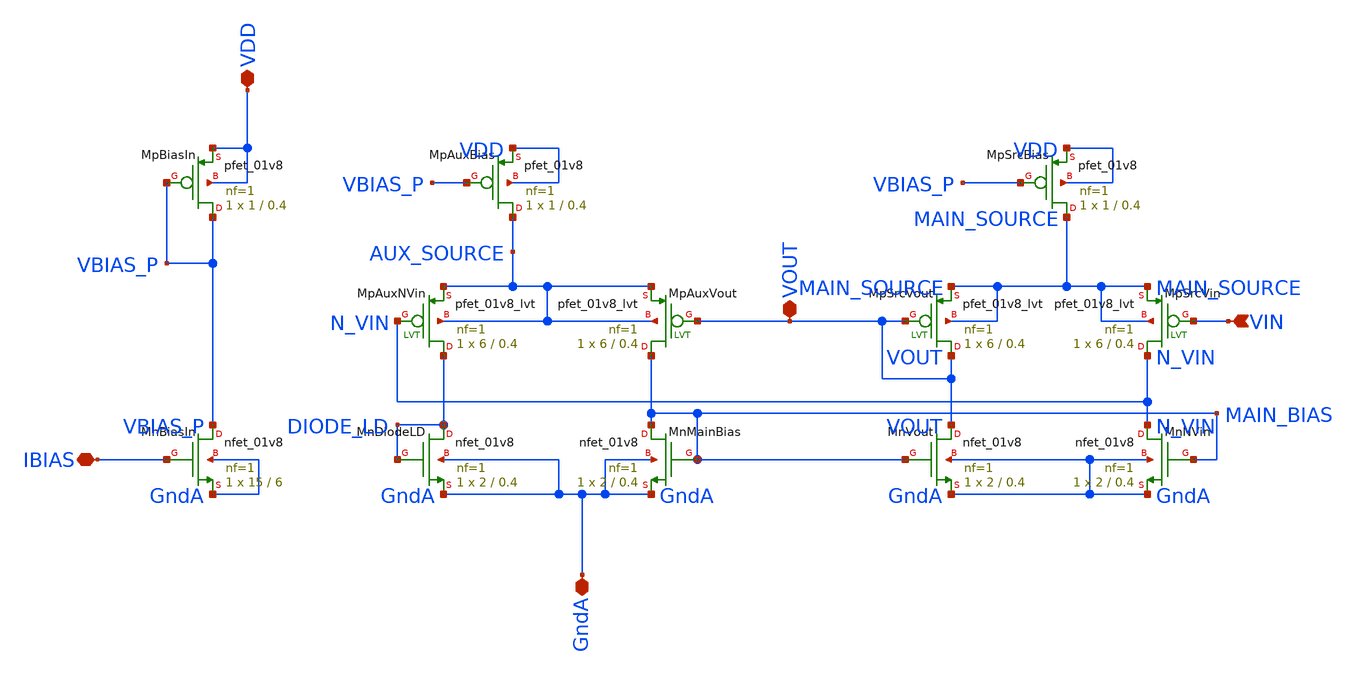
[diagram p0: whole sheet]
** sch_path: analog/xschem/infiniamp_xl_layout.sch
**.subckt infiniamp_xl_layout VDD GndA VIN IBIAS VOUT
*.iopin VDD
*.iopin GndA
*.ipin VIN
*.iopin IBIAS
*.iopin VOUT
XMpBiasIn VBIAS_P VBIAS_P VDD VDD sky130_fd_pr__pfet_01v8 L=0.4 W=1 nf=1 ad='int((1 + 1)/2) * 1 / 1 * 0.29'
+ as='int((1 + 2)/2) * 1 / 1 * 0.29' pd='2*int((1 + 1)/2) * (1 / 1 + 0.29)' ps='2*int((1 + 2)/2) * (1 / 1 + 0.29)'
+ nrd='0.29 / 1 ' nrs='0.29 / 1 ' sa=0 sb=0 sd=0 mult=1 m=1
XMpAuxBias AUX_SOURCE VBIAS_P VDD VDD sky130_fd_pr__pfet_01v8 L=0.4 W=1 nf=1 ad='int((1 + 1)/2) * 1 / 1 * 0.29'
+ as='int((1 + 2)/2) * 1 / 1 * 0.29' pd='2*int((1 + 1)/2) * (1 / 1 + 0.29)' ps='2*int((1 + 2)/2) * (1 / 1 + 0.29)'
+ nrd='0.29 / 1 ' nrs='0.29 / 1 ' sa=0 sb=0 sd=0 mult=1 m=1
XMpSrcBias MAIN_SOURCE VBIAS_P VDD VDD sky130_fd_pr__pfet_01v8 L=0.4 W=1 nf=1 ad='int((1 + 1)/2) * 1 / 1 * 0.29'
+ as='int((1 + 2)/2) * 1 / 1 * 0.29' pd='2*int((1 + 1)/2) * (1 / 1 + 0.29)' ps='2*int((1 + 2)/2) * (1 / 1 + 0.29)'
+ nrd='0.29 / 1 ' nrs='0.29 / 1 ' sa=0 sb=0 sd=0 mult=1 m=1
XMpAuxNVin DIODE_LD N_VIN AUX_SOURCE AUX_SOURCE sky130_fd_pr__pfet_01v8_lvt L=0.4 W=6 nf=1 ad='int((1 + 1)/2) * 6 / 1 * 0.29'
+ as='int((1 + 2)/2) * 6 / 1 * 0.29' pd='2*int((1 + 1)/2) * (6 / 1 + 0.29)' ps='2*int((1 + 2)/2) * (6 / 1 + 0.29)'
+ nrd='0.29 / 6 ' nrs='0.29 / 6 ' sa=0 sb=0 sd=0 mult=1 m=1
XMpAuxVout MAIN_BIAS VOUT AUX_SOURCE AUX_SOURCE sky130_fd_pr__pfet_01v8_lvt L=0.4 W=6 nf=1 ad='int((1 + 1)/2) * 6 / 1 * 0.29'
+ as='int((1 + 2)/2) * 6 / 1 * 0.29' pd='2*int((1 + 1)/2) * (6 / 1 + 0.29)' ps='2*int((1 + 2)/2) * (6 / 1 + 0.29)'
+ nrd='0.29 / 6 ' nrs='0.29 / 6 ' sa=0 sb=0 sd=0 mult=1 m=1
XMpSrcVin N_VIN VIN MAIN_SOURCE MAIN_SOURCE sky130_fd_pr__pfet_01v8_lvt L=0.4 W=6 nf=1 ad='int((1 + 1)/2) * 6 / 1 * 0.29'
+ as='int((1 + 2)/2) * 6 / 1 * 0.29' pd='2*int((1 + 1)/2) * (6 / 1 + 0.29)' ps='2*int((1 + 2)/2) * (6 / 1 + 0.29)'
+ nrd='0.29 / 6 ' nrs='0.29 / 6 ' sa=0 sb=0 sd=0 mult=1 m=1
XMpSrcVout VOUT VOUT MAIN_SOURCE MAIN_SOURCE sky130_fd_pr__pfet_01v8_lvt L=0.4 W=6 nf=1 ad='int((1 + 1)/2) * 6 / 1 * 0.29'
+ as='int((1 + 2)/2) * 6 / 1 * 0.29' pd='2*int((1 + 1)/2) * (6 / 1 + 0.29)' ps='2*int((1 + 2)/2) * (6 / 1 + 0.29)'
+ nrd='0.29 / 6 ' nrs='0.29 / 6 ' sa=0 sb=0 sd=0 mult=1 m=1
XMnBiasIn VBIAS_P IBIAS GndA GndA sky130_fd_pr__nfet_01v8 L=6 W=15 nf=1 ad='int((1 + 1)/2) * 15 / 1 * 0.29'
+ as='int((1 + 2)/2) * 15 / 1 * 0.29' pd='2*int((1 + 1)/2) * (15 / 1 + 0.29)' ps='2*int((1 + 2)/2) * (15 / 1 + 0.29)'
+ nrd='0.29 / 15 ' nrs='0.29 / 15 ' sa=0 sb=0 sd=0 mult=1 m=1
XMnDiodeLD DIODE_LD DIODE_LD GndA GndA sky130_fd_pr__nfet_01v8 L=0.4 W=2 nf=1 ad='int((1 + 1)/2) * 2 / 1 * 0.29'
+ as='int((1 + 2)/2) * 2 / 1 * 0.29' pd='2*int((1 + 1)/2) * (2 / 1 + 0.29)' ps='2*int((1 + 2)/2) * (2 / 1 + 0.29)'
+ nrd='0.29 / 2 ' nrs='0.29 / 2 ' sa=0 sb=0 sd=0 mult=1 m=1
XMnMainBias MAIN_BIAS MAIN_BIAS GndA GndA sky130_fd_pr__nfet_01v8 L=0.4 W=2 nf=1 ad='int((1 + 1)/2) * 2 / 1 * 0.29'
+ as='int((1 + 2)/2) * 2 / 1 * 0.29' pd='2*int((1 + 1)/2) * (2 / 1 + 0.29)' ps='2*int((1 + 2)/2) * (2 / 1 + 0.29)'
+ nrd='0.29 / 2 ' nrs='0.29 / 2 ' sa=0 sb=0 sd=0 mult=1 m=1
XMnNVin N_VIN MAIN_BIAS GndA GndA sky130_fd_pr__nfet_01v8 L=0.4 W=2 nf=1 ad='int((1 + 1)/2) * 2 / 1 * 0.29'
+ as='int((1 + 2)/2) * 2 / 1 * 0.29' pd='2*int((1 + 1)/2) * (2 / 1 + 0.29)' ps='2*int((1 + 2)/2) * (2 / 1 + 0.29)'
+ nrd='0.29 / 2 ' nrs='0.29 / 2 ' sa=0 sb=0 sd=0 mult=1 m=1
XMnVout VOUT MAIN_BIAS GndA GndA sky130_fd_pr__nfet_01v8 L=0.4 W=2 nf=1 ad='int((1 + 1)/2) * 2 / 1 * 0.29'
+ as='int((1 + 2)/2) * 2 / 1 * 0.29' pd='2*int((1 + 1)/2) * (2 / 1 + 0.29)' ps='2*int((1 + 2)/2) * (2 / 1 + 0.29)'
+ nrd='0.29 / 2 ' nrs='0.29 / 2 ' sa=0 sb=0 sd=0 mult=1 m=1
**.ends
.end
